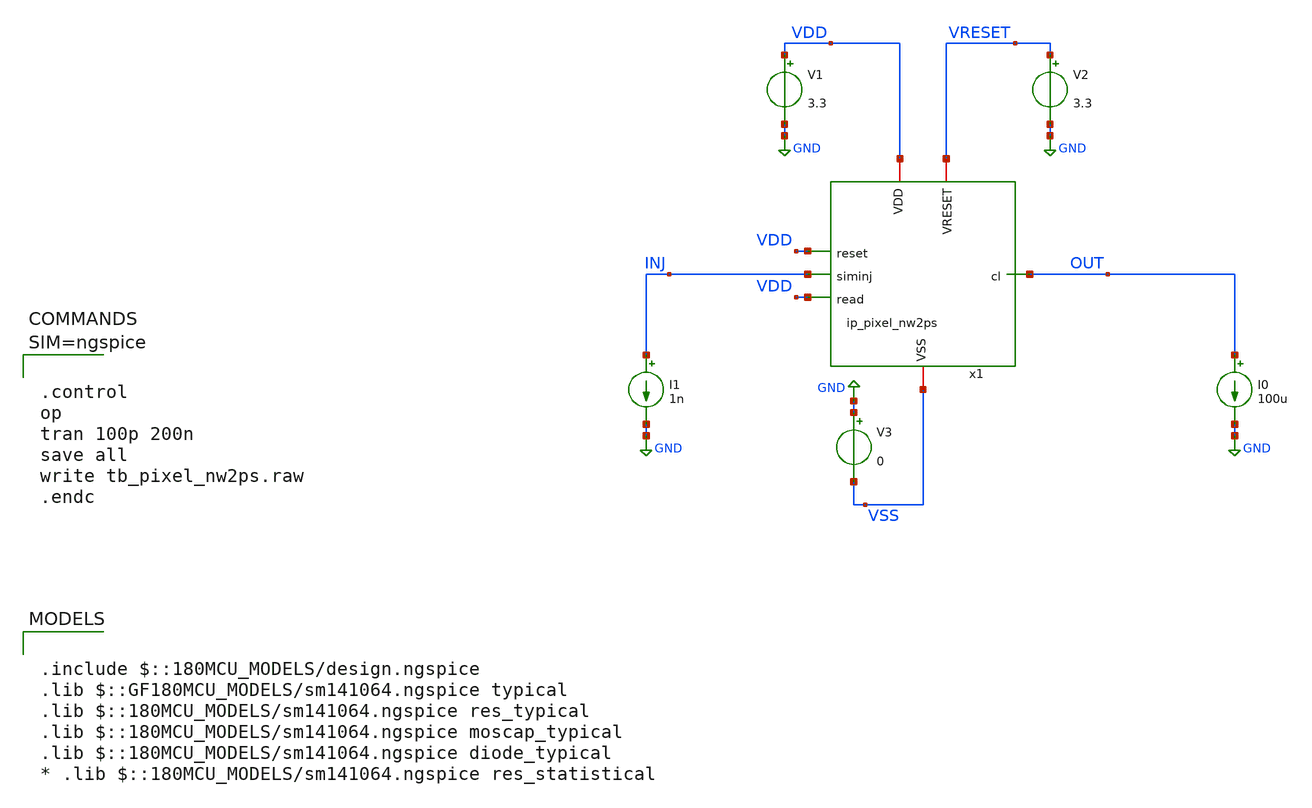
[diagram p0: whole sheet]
** sch_path: xschem/tb_pixel_nw2ps.sch
**.subckt tb_pixel_nw2ps
V1 VDD GND 3.3
V2 VRESET GND 3.3
V3 GND VSS 0
I0 OUT GND 100u
I1 INJ GND 1n
x1 VDD VRESET VDD INJ OUT VDD VSS ip_pixel_nw2ps
**** begin user architecture code

.include $::180MCU_MODELS/design.ngspice
.lib $::GF180MCU_MODELS/sm141064.ngspice typical
.lib $::180MCU_MODELS/sm141064.ngspice res_typical
.lib $::180MCU_MODELS/sm141064.ngspice moscap_typical
.lib $::180MCU_MODELS/sm141064.ngspice diode_typical
* .lib $::180MCU_MODELS/sm141064.ngspice res_statistical




.control
op
tran 100p 200n
save all
write tb_pixel_nw2ps.raw
.endc



**** end user architecture code
**.ends

* expanding   symbol:  ip_pixel_nw2ps.sym # of pins=7
** sym_path: xschem/ip_pixel_nw2ps.sym
** sch_path: xschem/ip_pixel_nw2ps.sch
.subckt ip_pixel_nw2ps VDD VRESET reset siminj cl read VSS
*.iopin VDD
*.iopin VSS
*.ipin siminj
*.ipin reset
*.ipin read
*.iopin VRESET
*.opin cl
XM1 VRESET reset siminj VSS nfet_03v3 L=0.28u W=0.22u nf=1 ad='int((nf+1)/2) * W/nf * 0.18u' as='int((nf+2)/2) * W/nf * 0.18u'
+ pd='2*int((nf+1)/2) * (W/nf + 0.18u)' ps='2*int((nf+2)/2) * (W/nf + 0.18u)' nrd='0.18u / W' nrs='0.18u / W'
+ sa=0 sb=0 sd=0 m=1
XM2 VDD siminj net1 VSS nfet_03v3 L=0.28u W=0.22u nf=1 ad='int((nf+1)/2) * W/nf * 0.18u' as='int((nf+2)/2) * W/nf * 0.18u'
+ pd='2*int((nf+1)/2) * (W/nf + 0.18u)' ps='2*int((nf+2)/2) * (W/nf + 0.18u)' nrd='0.18u / W' nrs='0.18u / W'
+ sa=0 sb=0 sd=0 m=1
XM3 net1 read cl VSS nfet_03v3 L=0.28u W=0.22u nf=1 ad='int((nf+1)/2) * W/nf * 0.18u' as='int((nf+2)/2) * W/nf * 0.18u'
+ pd='2*int((nf+1)/2) * (W/nf + 0.18u)' ps='2*int((nf+2)/2) * (W/nf + 0.18u)' nrd='0.18u / W' nrs='0.18u / W'
+ sa=0 sb=0 sd=0 m=1
D1 VSS siminj diode_nd2ps_03v3 w=12u l=10u area='12u * 10u ' pj='2*12u + 2*10u ' m=1
.ends

.GLOBAL GND
.end
